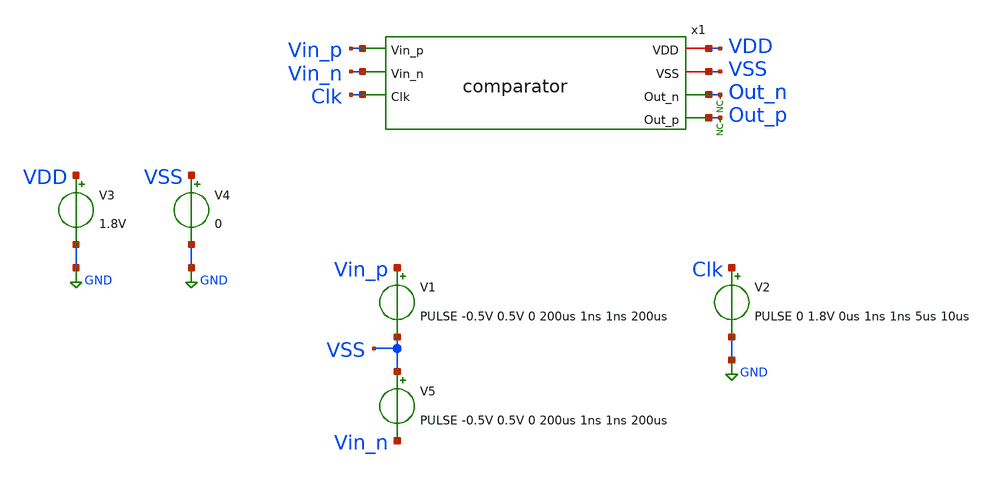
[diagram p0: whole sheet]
** sch_path: xschem/tests/comparator/comparator_test_small_input_v.sch
**.subckt comparator_test_small_input_v
V3 VDD GND 1.8V
V4 VSS GND 0
x1 VDD VSS Vin_p Out_n Vin_n Out_p Clk comparator
V1 Vin_p VSS PULSE -0.5V 0.5V 0 200us 1ns 1ns 200us
V2 Clk GND PULSE 0 1.8V 0us 1ns 1ns 5us 10us
* noconn Out_p
* noconn Out_n
V5 VSS Vin_n PULSE -0.5V 0.5V 0 200us 1ns 1ns 200us
**** begin user architecture code
 .lib $::SKYWATER_MODELS/sky130.lib.spice tt
.include $::SKYWATER_STDCELLS/sky130_fd_sc_hd.spice


.options acct list
.temp 25
*vvcc VDD 0 dc 1.8
*vvss VSS 0 0
.control
tran 0.1u 200u
*dc V1 0 1.8V 0.1
plot Vin_p-Vin_n Out_p-Out_n Clk-4
plot Vin_p-Vin_n x1.pre_amp_p-x1.pre_amp_n Clk-4
write comparator_test_small_input_v.raw
.endc


**** end user architecture code
**.ends

* expanding   symbol:  src/comparator/comparator.sym # of pins=7
** sym_path: xschem/src/comparator/comparator.sym
** sch_path: xschem/src/comparator/comparator.sch
.subckt comparator VDD VSS Vin_p Out_n Vin_n Out_p Clk
*.iopin VDD
*.iopin VSS
*.ipin Vin_p
*.opin Out_n
*.ipin Vin_n
*.opin Out_p
*.ipin Clk
XM1 Pre_Amp_p Clk VDD VDD sky130_fd_pr__pfet_01v8 L=1 W=88.2 nf=2 ad='int((nf+1)/2) * W/nf * 0.29' as='int((nf+2)/2) * W/nf * 0.29'
+ pd='2*int((nf+1)/2) * (W/nf + 0.29)' ps='2*int((nf+2)/2) * (W/nf + 0.29)' nrd='0.29 / W' nrs='0.29 / W'
+ sa=0 sb=0 sd=0 mult=1 m=1
XM2 Pre_Amp_n Clk VDD VDD sky130_fd_pr__pfet_01v8 L=1 W=88.2 nf=2 ad='int((nf+1)/2) * W/nf * 0.29' as='int((nf+2)/2) * W/nf * 0.29'
+ pd='2*int((nf+1)/2) * (W/nf + 0.29)' ps='2*int((nf+2)/2) * (W/nf + 0.29)' nrd='0.29 / W' nrs='0.29 / W'
+ sa=0 sb=0 sd=0 mult=1 m=1
XM3 Pre_Amp_n Vin_p net1 VSS sky130_fd_pr__nfet_01v8 L=0.15 W=100 nf=2 ad='int((nf+1)/2) * W/nf * 0.29'
+ as='int((nf+2)/2) * W/nf * 0.29' pd='2*int((nf+1)/2) * (W/nf + 0.29)' ps='2*int((nf+2)/2) * (W/nf + 0.29)'
+ nrd='0.29 / W' nrs='0.29 / W' sa=0 sb=0 sd=0 mult=1 m=1
XM4 Pre_Amp_p Vin_n net1 VSS sky130_fd_pr__nfet_01v8 L=0.15 W=100 nf=2 ad='int((nf+1)/2) * W/nf * 0.29'
+ as='int((nf+2)/2) * W/nf * 0.29' pd='2*int((nf+1)/2) * (W/nf + 0.29)' ps='2*int((nf+2)/2) * (W/nf + 0.29)'
+ nrd='0.29 / W' nrs='0.29 / W' sa=0 sb=0 sd=0 mult=1 m=1
XM5 net3 Out_p VDD VDD sky130_fd_pr__pfet_01v8 L=0.15 W=1.605 nf=1 ad='int((nf+1)/2) * W/nf * 0.29' as='int((nf+2)/2) * W/nf * 0.29'
+ pd='2*int((nf+1)/2) * (W/nf + 0.29)' ps='2*int((nf+2)/2) * (W/nf + 0.29)' nrd='0.29 / W' nrs='0.29 / W'
+ sa=0 sb=0 sd=0 mult=16 m=16
XM6 net2 Out_n VDD VDD sky130_fd_pr__pfet_01v8 L=0.15 W=1.605 nf=1 ad='int((nf+1)/2) * W/nf * 0.29' as='int((nf+2)/2) * W/nf * 0.29'
+ pd='2*int((nf+1)/2) * (W/nf + 0.29)' ps='2*int((nf+2)/2) * (W/nf + 0.29)' nrd='0.29 / W' nrs='0.29 / W'
+ sa=0 sb=0 sd=0 mult=16 m=16
XM9 net1 Clk VSS VSS sky130_fd_pr__nfet_01v8 L=1 W=50 nf=5 ad='int((nf+1)/2) * W/nf * 0.29' as='int((nf+2)/2) * W/nf * 0.29'
+ pd='2*int((nf+1)/2) * (W/nf + 0.29)' ps='2*int((nf+2)/2) * (W/nf + 0.29)' nrd='0.29 / W' nrs='0.29 / W'
+ sa=0 sb=0 sd=0 mult=4 m=4
XM11 Out_n Clk_n VSS VSS sky130_fd_pr__nfet_01v8 L=0.15 W=0.91 nf=1 ad='int((nf+1)/2) * W/nf * 0.29'
+ as='int((nf+2)/2) * W/nf * 0.29' pd='2*int((nf+1)/2) * (W/nf + 0.29)' ps='2*int((nf+2)/2) * (W/nf + 0.29)'
+ nrd='0.29 / W' nrs='0.29 / W' sa=0 sb=0 sd=0 mult=16 m=16
XM12 Out_n Out_p VSS VSS sky130_fd_pr__nfet_01v8 L=0.15 W=0.91 nf=1 ad='int((nf+1)/2) * W/nf * 0.29'
+ as='int((nf+2)/2) * W/nf * 0.29' pd='2*int((nf+1)/2) * (W/nf + 0.29)' ps='2*int((nf+2)/2) * (W/nf + 0.29)'
+ nrd='0.29 / W' nrs='0.29 / W' sa=0 sb=0 sd=0 mult=16 m=16
XM13 Out_p Out_n VSS VSS sky130_fd_pr__nfet_01v8 L=0.15 W=0.91 nf=1 ad='int((nf+1)/2) * W/nf * 0.29'
+ as='int((nf+2)/2) * W/nf * 0.29' pd='2*int((nf+1)/2) * (W/nf + 0.29)' ps='2*int((nf+2)/2) * (W/nf + 0.29)'
+ nrd='0.29 / W' nrs='0.29 / W' sa=0 sb=0 sd=0 mult=16 m=16
XM14 Out_p Clk_n VSS VSS sky130_fd_pr__nfet_01v8 L=0.15 W=0.91 nf=1 ad='int((nf+1)/2) * W/nf * 0.29'
+ as='int((nf+2)/2) * W/nf * 0.29' pd='2*int((nf+1)/2) * (W/nf + 0.29)' ps='2*int((nf+2)/2) * (W/nf + 0.29)'
+ nrd='0.29 / W' nrs='0.29 / W' sa=0 sb=0 sd=0 mult=16 m=16
XM15 Clk_n Clk VDD VDD sky130_fd_pr__pfet_01v8 L=0.15 W=1.605 nf=1 ad='int((nf+1)/2) * W/nf * 0.29' as='int((nf+2)/2) * W/nf * 0.29'
+ pd='2*int((nf+1)/2) * (W/nf + 0.29)' ps='2*int((nf+2)/2) * (W/nf + 0.29)' nrd='0.29 / W' nrs='0.29 / W'
+ sa=0 sb=0 sd=0 mult=1 m=1
XM16 Clk_n Clk VSS VSS sky130_fd_pr__nfet_01v8 L=0.15 W=0.910 nf=1 ad='int((nf+1)/2) * W/nf * 0.29' as='int((nf+2)/2) * W/nf * 0.29'
+ pd='2*int((nf+1)/2) * (W/nf + 0.29)' ps='2*int((nf+2)/2) * (W/nf + 0.29)' nrd='0.29 / W' nrs='0.29 / W'
+ sa=0 sb=0 sd=0 mult=1 m=1
XM7 Out_p Pre_Amp_n net2 VDD sky130_fd_pr__pfet_01v8 L=0.15 W=1.605 nf=1 ad='int((nf+1)/2) * W/nf * 0.29'
+ as='int((nf+2)/2) * W/nf * 0.29' pd='2*int((nf+1)/2) * (W/nf + 0.29)' ps='2*int((nf+2)/2) * (W/nf + 0.29)'
+ nrd='0.29 / W' nrs='0.29 / W' sa=0 sb=0 sd=0 mult=16 m=16
XM8 Out_n Pre_Amp_p net3 VDD sky130_fd_pr__pfet_01v8 L=0.15 W=1.605 nf=1 ad='int((nf+1)/2) * W/nf * 0.29'
+ as='int((nf+2)/2) * W/nf * 0.29' pd='2*int((nf+1)/2) * (W/nf + 0.29)' ps='2*int((nf+2)/2) * (W/nf + 0.29)'
+ nrd='0.29 / W' nrs='0.29 / W' sa=0 sb=0 sd=0 mult=16 m=16
.ends

.GLOBAL GND
.end
